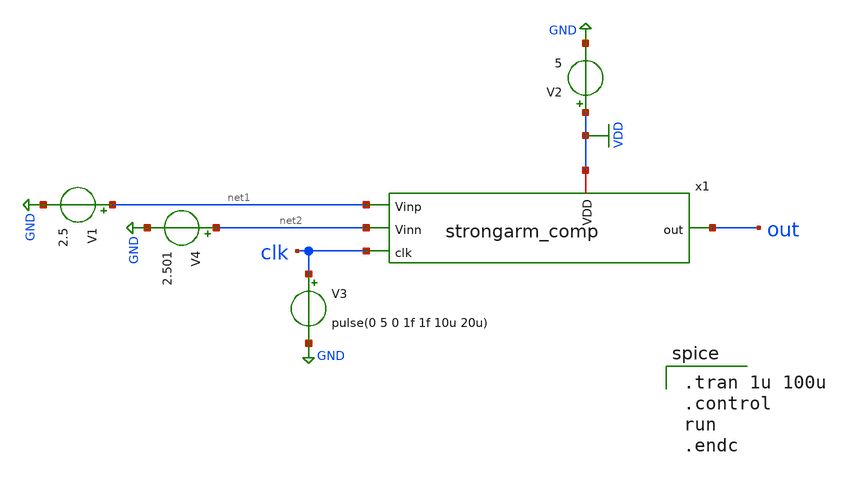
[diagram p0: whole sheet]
** sch_path: ADC/16bit_C2C/MagicAndSpice/strongarm_comp_TB.sch
**.subckt strongarm_comp_TB
x1 out net1 net2 VDD clk strongarm_comp
V3 clk GND pulse(0 5 0 1f 1f 10u 20u)
V2 VDD GND 5
V1 net1 GND 2.5
V4 net2 GND 2.501
**** begin user architecture code

** opencircuitdesign pdks install
.lib $::SKYWATER_MODELS/sky130.lib.spice tt



.tran 1u 100u
.control
run
.endc

**** end user architecture code
**.ends

* expanding   symbol:  /home/ee431/workspace/6SAR_CDAC/strongarm_comp.sym # of pins=5
** sym_path: ADC/16bit_C2C/MagicAndSpice/strongarm_comp.sym
** sch_path: ADC/16bit_C2C/MagicAndSpice/strongarm_comp.sch
.subckt strongarm_comp out Vinp Vinn VDD clk
*.ipin Vinp
*.ipin Vinn
*.ipin clk
*.iopin VDD
*.opin out
XM1 x out p GND sky130_fd_pr__nfet_g5v0d10v5 L=0.5 W=10 nf=1 ad='int((nf+1)/2) * W/nf * 0.29' as='int((nf+2)/2) * W/nf * 0.29'
+ pd='2*int((nf+1)/2) * (W/nf + 0.29)' ps='2*int((nf+2)/2) * (W/nf + 0.29)' nrd='0.29 / W' nrs='0.29 / W'
+ sa=0 sb=0 sd=0 mult=1 m=1
XM2 x out VDD VDD sky130_fd_pr__pfet_g5v0d10v5 L=0.5 W=10 nf=1 ad='int((nf+1)/2) * W/nf * 0.29' as='int((nf+2)/2) * W/nf * 0.29'
+ pd='2*int((nf+1)/2) * (W/nf + 0.29)' ps='2*int((nf+2)/2) * (W/nf + 0.29)' nrd='0.29 / W' nrs='0.29 / W'
+ sa=0 sb=0 sd=0 mult=1 m=1
XM3 out x VDD VDD sky130_fd_pr__pfet_g5v0d10v5 L=0.5 W=10 nf=1 ad='int((nf+1)/2) * W/nf * 0.29' as='int((nf+2)/2) * W/nf * 0.29'
+ pd='2*int((nf+1)/2) * (W/nf + 0.29)' ps='2*int((nf+2)/2) * (W/nf + 0.29)' nrd='0.29 / W' nrs='0.29 / W'
+ sa=0 sb=0 sd=0 mult=1 m=1
XM4 out x q GND sky130_fd_pr__nfet_g5v0d10v5 L=0.5 W=10 nf=1 ad='int((nf+1)/2) * W/nf * 0.29' as='int((nf+2)/2) * W/nf * 0.29'
+ pd='2*int((nf+1)/2) * (W/nf + 0.29)' ps='2*int((nf+2)/2) * (W/nf + 0.29)' nrd='0.29 / W' nrs='0.29 / W'
+ sa=0 sb=0 sd=0 mult=1 m=1
XM5 p Vinp net1 GND sky130_fd_pr__nfet_g5v0d10v5 L=0.5 W=10 nf=1 ad='int((nf+1)/2) * W/nf * 0.29' as='int((nf+2)/2) * W/nf * 0.29'
+ pd='2*int((nf+1)/2) * (W/nf + 0.29)' ps='2*int((nf+2)/2) * (W/nf + 0.29)' nrd='0.29 / W' nrs='0.29 / W'
+ sa=0 sb=0 sd=0 mult=1 m=1
XM6 q Vinn net1 GND sky130_fd_pr__nfet_g5v0d10v5 L=0.5 W=10 nf=1 ad='int((nf+1)/2) * W/nf * 0.29' as='int((nf+2)/2) * W/nf * 0.29'
+ pd='2*int((nf+1)/2) * (W/nf + 0.29)' ps='2*int((nf+2)/2) * (W/nf + 0.29)' nrd='0.29 / W' nrs='0.29 / W'
+ sa=0 sb=0 sd=0 mult=1 m=1
XM7 net1 clk GND GND sky130_fd_pr__nfet_g5v0d10v5 L=0.5 W=10 nf=1 ad='int((nf+1)/2) * W/nf * 0.29' as='int((nf+2)/2) * W/nf * 0.29'
+ pd='2*int((nf+1)/2) * (W/nf + 0.29)' ps='2*int((nf+2)/2) * (W/nf + 0.29)' nrd='0.29 / W' nrs='0.29 / W'
+ sa=0 sb=0 sd=0 mult=1 m=1
XM9 out clk VDD VDD sky130_fd_pr__pfet_g5v0d10v5 L=0.5 W=10 nf=1 ad='int((nf+1)/2) * W/nf * 0.29' as='int((nf+2)/2) * W/nf * 0.29'
+ pd='2*int((nf+1)/2) * (W/nf + 0.29)' ps='2*int((nf+2)/2) * (W/nf + 0.29)' nrd='0.29 / W' nrs='0.29 / W'
+ sa=0 sb=0 sd=0 mult=1 m=1
XM10 x clk VDD VDD sky130_fd_pr__pfet_g5v0d10v5 L=0.5 W=10 nf=1 ad='int((nf+1)/2) * W/nf * 0.29' as='int((nf+2)/2) * W/nf * 0.29'
+ pd='2*int((nf+1)/2) * (W/nf + 0.29)' ps='2*int((nf+2)/2) * (W/nf + 0.29)' nrd='0.29 / W' nrs='0.29 / W'
+ sa=0 sb=0 sd=0 mult=1 m=1
XM8 p clk VDD VDD sky130_fd_pr__pfet_g5v0d10v5 L=0.5 W=10 nf=1 ad='int((nf+1)/2) * W/nf * 0.29' as='int((nf+2)/2) * W/nf * 0.29'
+ pd='2*int((nf+1)/2) * (W/nf + 0.29)' ps='2*int((nf+2)/2) * (W/nf + 0.29)' nrd='0.29 / W' nrs='0.29 / W'
+ sa=0 sb=0 sd=0 mult=1 m=1
XM11 q clk VDD VDD sky130_fd_pr__pfet_g5v0d10v5 L=0.5 W=10 nf=1 ad='int((nf+1)/2) * W/nf * 0.29' as='int((nf+2)/2) * W/nf * 0.29'
+ pd='2*int((nf+1)/2) * (W/nf + 0.29)' ps='2*int((nf+2)/2) * (W/nf + 0.29)' nrd='0.29 / W' nrs='0.29 / W'
+ sa=0 sb=0 sd=0 mult=1 m=1
.ends

.GLOBAL GND
.GLOBAL VDD
.end
